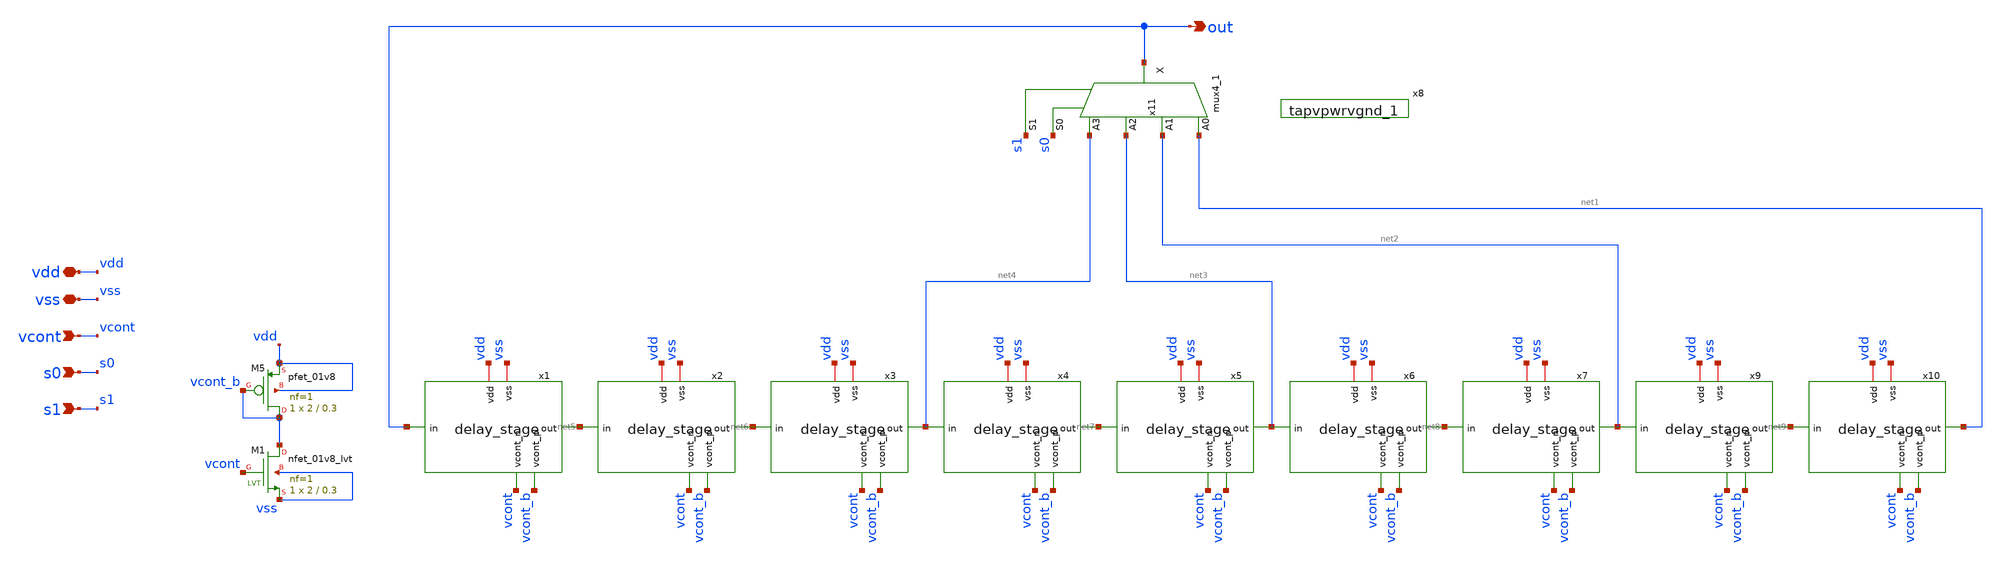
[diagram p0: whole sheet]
** sch_path: xschem/vco.sch
**.subckt vco vdd s0 s1 vcont vss out
*.iopin vdd
*.ipin s0
*.ipin s1
*.ipin vcont
*.iopin vss
*.opin out
x1 vdd vcont_b net5 out vcont vss delay_stage
x2 vdd vcont_b net6 net5 vcont vss delay_stage
x3 vdd vcont_b net4 net6 vcont vss delay_stage
x4 vdd vcont_b net7 net4 vcont vss delay_stage
x5 vdd vcont_b net3 net7 vcont vss delay_stage
x6 vdd vcont_b net8 net3 vcont vss delay_stage
x7 vdd vcont_b net2 net8 vcont vss delay_stage
x9 vdd vcont_b net9 net2 vcont vss delay_stage
x10 vdd vcont_b net1 net9 vcont vss delay_stage
x11 net1 net2 net3 net4 s0 s1 vss vss vdd vdd out sky130_fd_sc_hd__mux4_1
XM5 vcont_b vcont_b vdd vdd sky130_fd_pr__pfet_01v8 L=0.3 W=2 nf=1 ad='int((nf+1)/2) * W/nf * 0.29' as='int((nf+2)/2) * W/nf * 0.29'
+ pd='2*int((nf+1)/2) * (W/nf + 0.29)' ps='2*int((nf+2)/2) * (W/nf + 0.29)' nrd='0.29 / W' nrs='0.29 / W'
+ sa=0 sb=0 sd=0 mult=1 m=1
XM1 vcont_b vcont vss vss sky130_fd_pr__nfet_01v8_lvt L=0.3 W=2 nf=1 ad='int((nf+1)/2) * W/nf * 0.29'
+ as='int((nf+2)/2) * W/nf * 0.29' pd='2*int((nf+1)/2) * (W/nf + 0.29)' ps='2*int((nf+2)/2) * (W/nf + 0.29)'
+ nrd='0.29 / W' nrs='0.29 / W' sa=0 sb=0 sd=0 mult=1 m=1
x8 vss vdd sky130_fd_sc_hd__tapvpwrvgnd_1
**.ends

* expanding   symbol:  delay_stage.sym # of pins=6
** sym_path: xschem/delay_stage.sym
** sch_path: xschem/delay_stage.sch
.subckt delay_stage vdd vcont_p out in vcont_n vss
*.ipin in
*.opin out
*.iopin vdd
*.ipin vcont_n
*.ipin vcont_p
*.iopin vss
XM3 out in net2 vss sky130_fd_pr__nfet_01v8 L=0.45 W=1 nf=1 ad='int((nf+1)/2) * W/nf * 0.29' as='int((nf+2)/2) * W/nf * 0.29'
+ pd='2*int((nf+1)/2) * (W/nf + 0.29)' ps='2*int((nf+2)/2) * (W/nf + 0.29)' nrd='0.29 / W' nrs='0.29 / W'
+ sa=0 sb=0 sd=0 mult=1 m=1
XM2 out in net1 vdd sky130_fd_pr__pfet_01v8 L=0.45 W=2 nf=1 ad='int((nf+1)/2) * W/nf * 0.29' as='int((nf+2)/2) * W/nf * 0.29'
+ pd='2*int((nf+1)/2) * (W/nf + 0.29)' ps='2*int((nf+2)/2) * (W/nf + 0.29)' nrd='0.29 / W' nrs='0.29 / W'
+ sa=0 sb=0 sd=0 mult=1 m=1
XM1 net1 vcont_p vdd vdd sky130_fd_pr__pfet_01v8 L=0.45 W=2 nf=1 ad='int((nf+1)/2) * W/nf * 0.29' as='int((nf+2)/2) * W/nf * 0.29'
+ pd='2*int((nf+1)/2) * (W/nf + 0.29)' ps='2*int((nf+2)/2) * (W/nf + 0.29)' nrd='0.29 / W' nrs='0.29 / W'
+ sa=0 sb=0 sd=0 mult=1 m=1
XM4 net2 vcont_n vss vss sky130_fd_pr__nfet_01v8 L=0.45 W=1 nf=1 ad='int((nf+1)/2) * W/nf * 0.29' as='int((nf+2)/2) * W/nf * 0.29'
+ pd='2*int((nf+1)/2) * (W/nf + 0.29)' ps='2*int((nf+2)/2) * (W/nf + 0.29)' nrd='0.29 / W' nrs='0.29 / W'
+ sa=0 sb=0 sd=0 mult=1 m=1
.ends

.end
